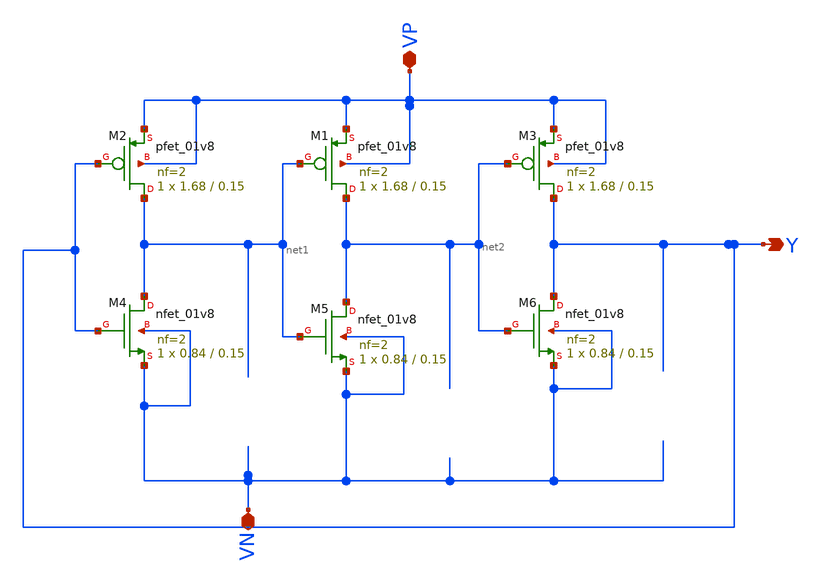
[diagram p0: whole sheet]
** sch_path: Week 3/Week 3/xschem 2/analog.sch
**.subckt analog VP VN Y
*.iopin VP
*.iopin VN
*.opin Y
XM2 net1 Y VP VP sky130_fd_pr__pfet_01v8 L=0.15 W=1.68 nf=2 ad='int((nf+1)/2) * W/nf * 0.29' as='int((nf+2)/2) * W/nf * 0.29'
+ pd='2*int((nf+1)/2) * (W/nf + 0.29)' ps='2*int((nf+2)/2) * (W/nf + 0.29)' nrd='0.29 / W' nrs='0.29 / W'
+ sa=0 sb=0 sd=0 mult=1 m=1
XM1 net2 net1 VP VP sky130_fd_pr__pfet_01v8 L=0.15 W=1.68 nf=2 ad='int((nf+1)/2) * W/nf * 0.29' as='int((nf+2)/2) * W/nf * 0.29'
+ pd='2*int((nf+1)/2) * (W/nf + 0.29)' ps='2*int((nf+2)/2) * (W/nf + 0.29)' nrd='0.29 / W' nrs='0.29 / W'
+ sa=0 sb=0 sd=0 mult=1 m=1
XM3 Y net2 VP VP sky130_fd_pr__pfet_01v8 L=0.15 W=1.68 nf=2 ad='int((nf+1)/2) * W/nf * 0.29' as='int((nf+2)/2) * W/nf * 0.29'
+ pd='2*int((nf+1)/2) * (W/nf + 0.29)' ps='2*int((nf+2)/2) * (W/nf + 0.29)' nrd='0.29 / W' nrs='0.29 / W'
+ sa=0 sb=0 sd=0 mult=1 m=1
XM4 net1 Y VN VN sky130_fd_pr__nfet_01v8 L=0.15 W=0.84 nf=2 ad='int((nf+1)/2) * W/nf * 0.29' as='int((nf+2)/2) * W/nf * 0.29'
+ pd='2*int((nf+1)/2) * (W/nf + 0.29)' ps='2*int((nf+2)/2) * (W/nf + 0.29)' nrd='0.29 / W' nrs='0.29 / W'
+ sa=0 sb=0 sd=0 mult=1 m=1
XM5 net2 net1 VN VN sky130_fd_pr__nfet_01v8 L=0.15 W=0.84 nf=2 ad='int((nf+1)/2) * W/nf * 0.29' as='int((nf+2)/2) * W/nf * 0.29'
+ pd='2*int((nf+1)/2) * (W/nf + 0.29)' ps='2*int((nf+2)/2) * (W/nf + 0.29)' nrd='0.29 / W' nrs='0.29 / W'
+ sa=0 sb=0 sd=0 mult=1 m=1
XM6 Y net2 VN VN sky130_fd_pr__nfet_01v8 L=0.15 W=0.84 nf=2 ad='int((nf+1)/2) * W/nf * 0.29' as='int((nf+2)/2) * W/nf * 0.29'
+ pd='2*int((nf+1)/2) * (W/nf + 0.29)' ps='2*int((nf+2)/2) * (W/nf + 0.29)' nrd='0.29 / W' nrs='0.29 / W'
+ sa=0 sb=0 sd=0 mult=1 m=1
**.ends
.end
